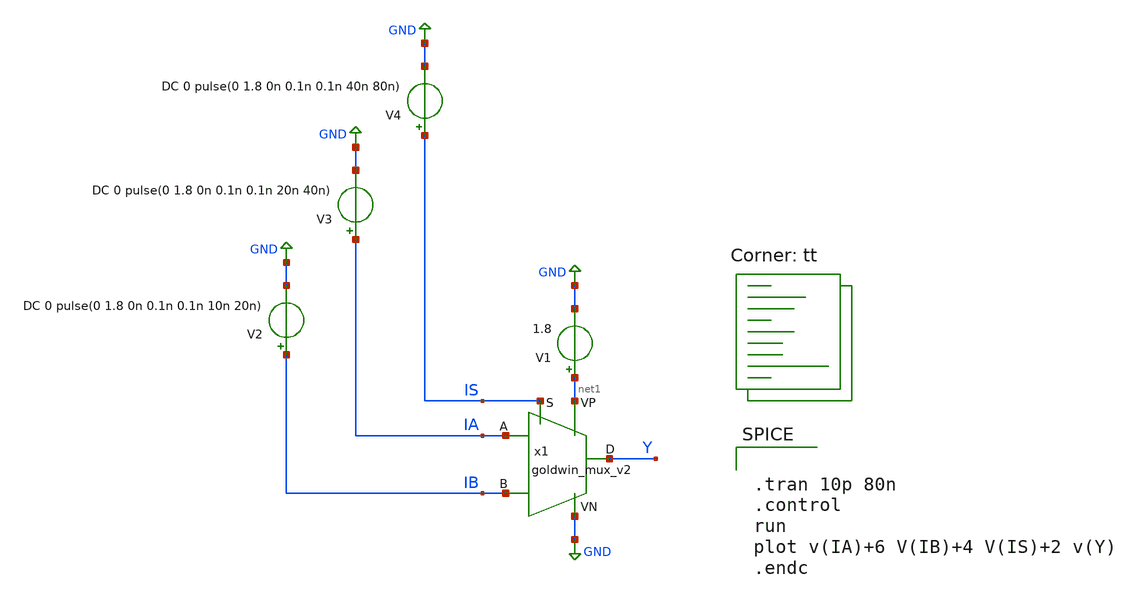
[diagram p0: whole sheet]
** sch_path: APIC-UTS/schematic/goldwin_mux_v2/tb_goldwin_mux_v2.sch
**.subckt tb_goldwin_mux_v2
V1 net1 GND 1.8
V2 IB GND DC 0 pulse(0 1.8 0n 0.1n 0.1n 10n 20n)
V3 IA GND DC 0 pulse(0 1.8 0n 0.1n 0.1n 20n 40n)
V4 IS GND DC 0 pulse(0 1.8 0n 0.1n 0.1n 40n 80n)
x1 IA IB IS Y net1 GND goldwin_mux_v2
**** begin user architecture code


.tran 10p 80n
.control
run
plot v(IA)+6 V(IB)+4 V(IS)+2 v(Y)
.endc


.lib $::SKYWATER_MODELS/sky130.lib.spice tt
**** end user architecture code
**.ends
.GLOBAL GND
.end
